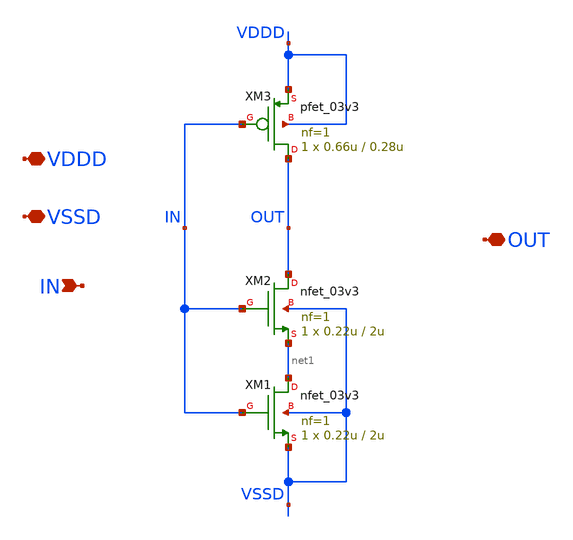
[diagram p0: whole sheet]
** sch_path: SAR_ADC/blocks/SAR_clock/clock_generator_delay_cell.sch
**.subckt clock_generator_delay_cell VDDD VSSD IN OUT
*.iopin VDDD
*.iopin VSSD
*.ipin IN
*.iopin OUT
XM1 net1 IN VSSD VSSD nfet_03v3 L=2u W=0.22u nf=1 ad='int((nf+1)/2) * W/nf * 0.18u' as='int((nf+2)/2) * W/nf * 0.18u'
+ pd='2*int((nf+1)/2) * (W/nf + 0.18u)' ps='2*int((nf+2)/2) * (W/nf + 0.18u)' nrd='0.18u / W' nrs='0.18u / W'
+ sa=0 sb=0 sd=0 m=1
XM2 OUT IN net1 VSSD nfet_03v3 L=2u W=0.22u nf=1 ad='int((nf+1)/2) * W/nf * 0.18u' as='int((nf+2)/2) * W/nf * 0.18u'
+ pd='2*int((nf+1)/2) * (W/nf + 0.18u)' ps='2*int((nf+2)/2) * (W/nf + 0.18u)' nrd='0.18u / W' nrs='0.18u / W'
+ sa=0 sb=0 sd=0 m=1
XM3 OUT IN VDDD VDDD pfet_03v3 L=0.28u W=0.66u nf=1 ad='int((nf+1)/2) * W/nf * 0.18u' as='int((nf+2)/2) * W/nf * 0.18u'
+ pd='2*int((nf+1)/2) * (W/nf + 0.18u)' ps='2*int((nf+2)/2) * (W/nf + 0.18u)' nrd='0.18u / W' nrs='0.18u / W'
+ sa=0 sb=0 sd=0 m=1
**.ends
.end
